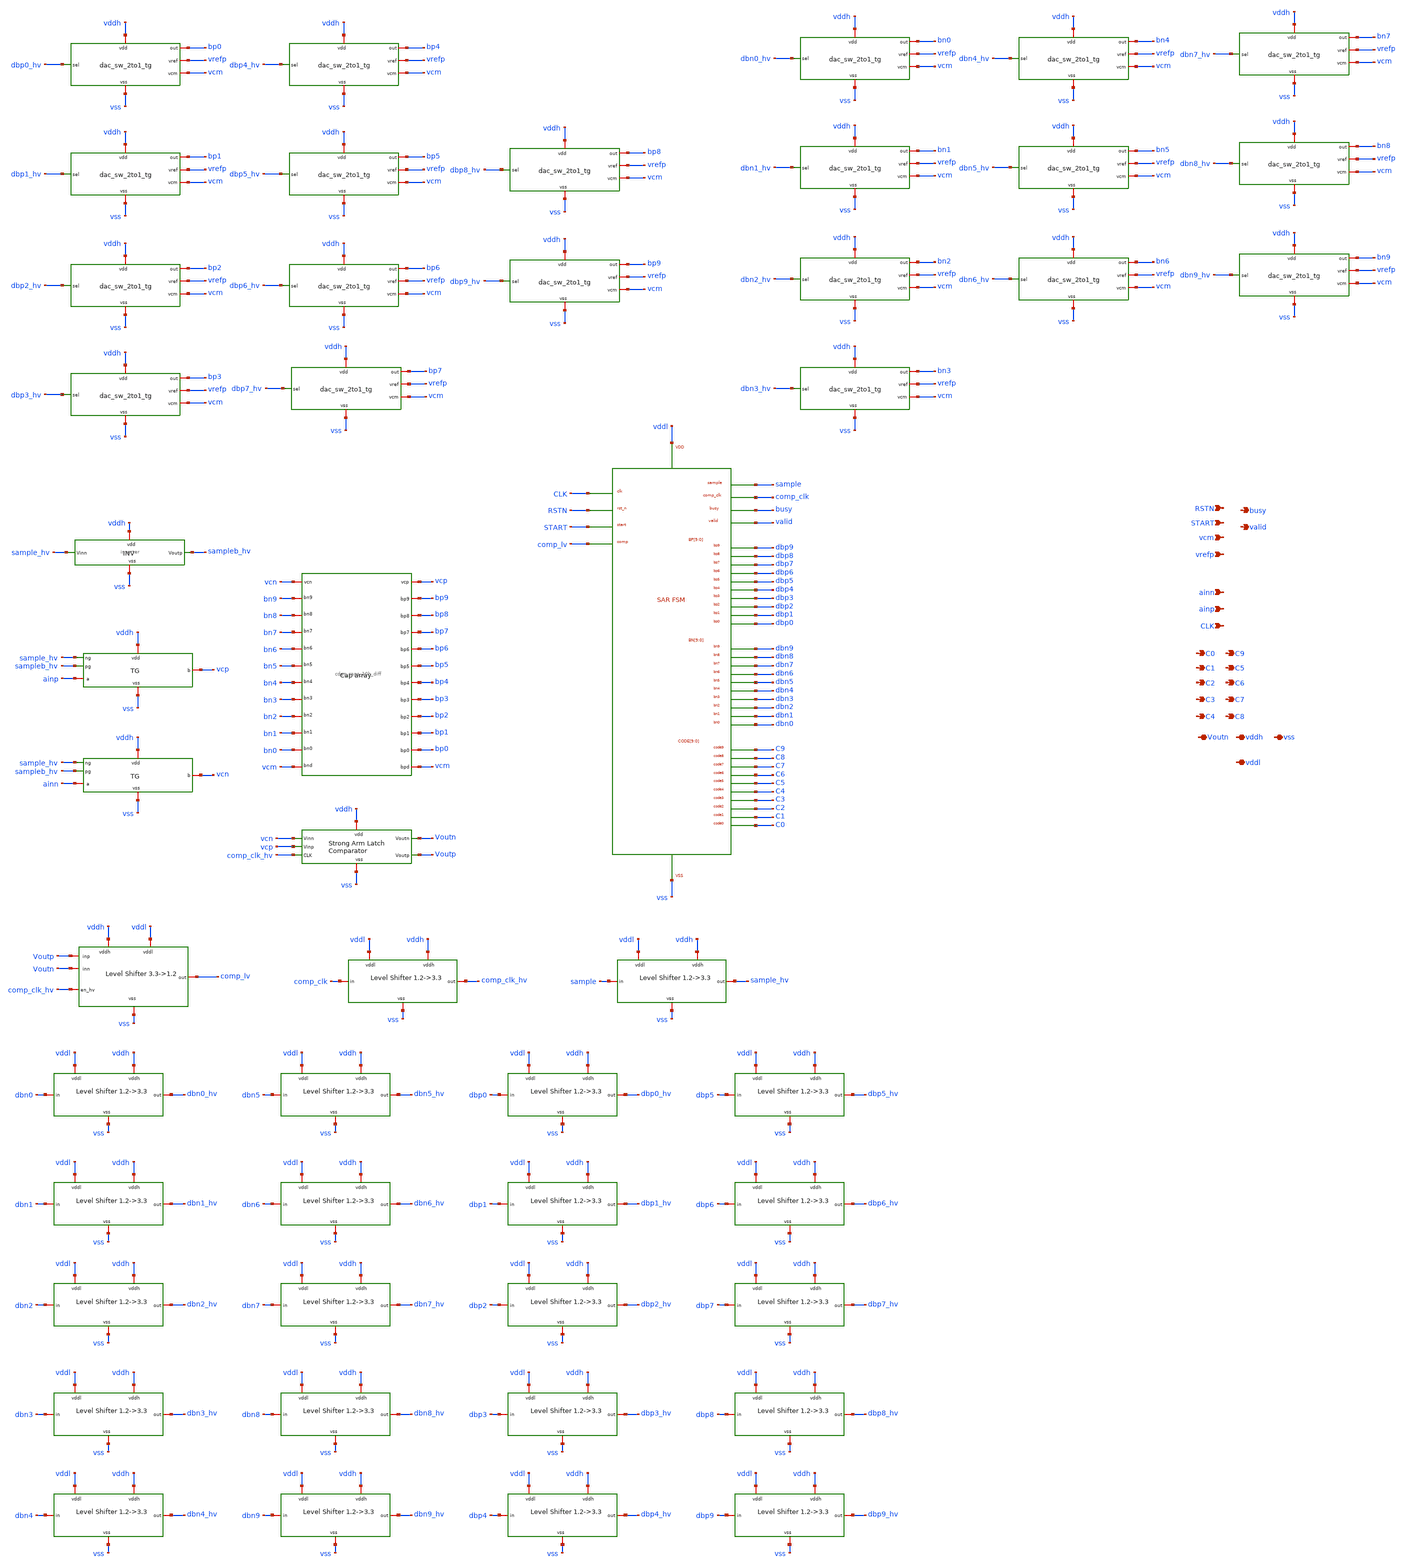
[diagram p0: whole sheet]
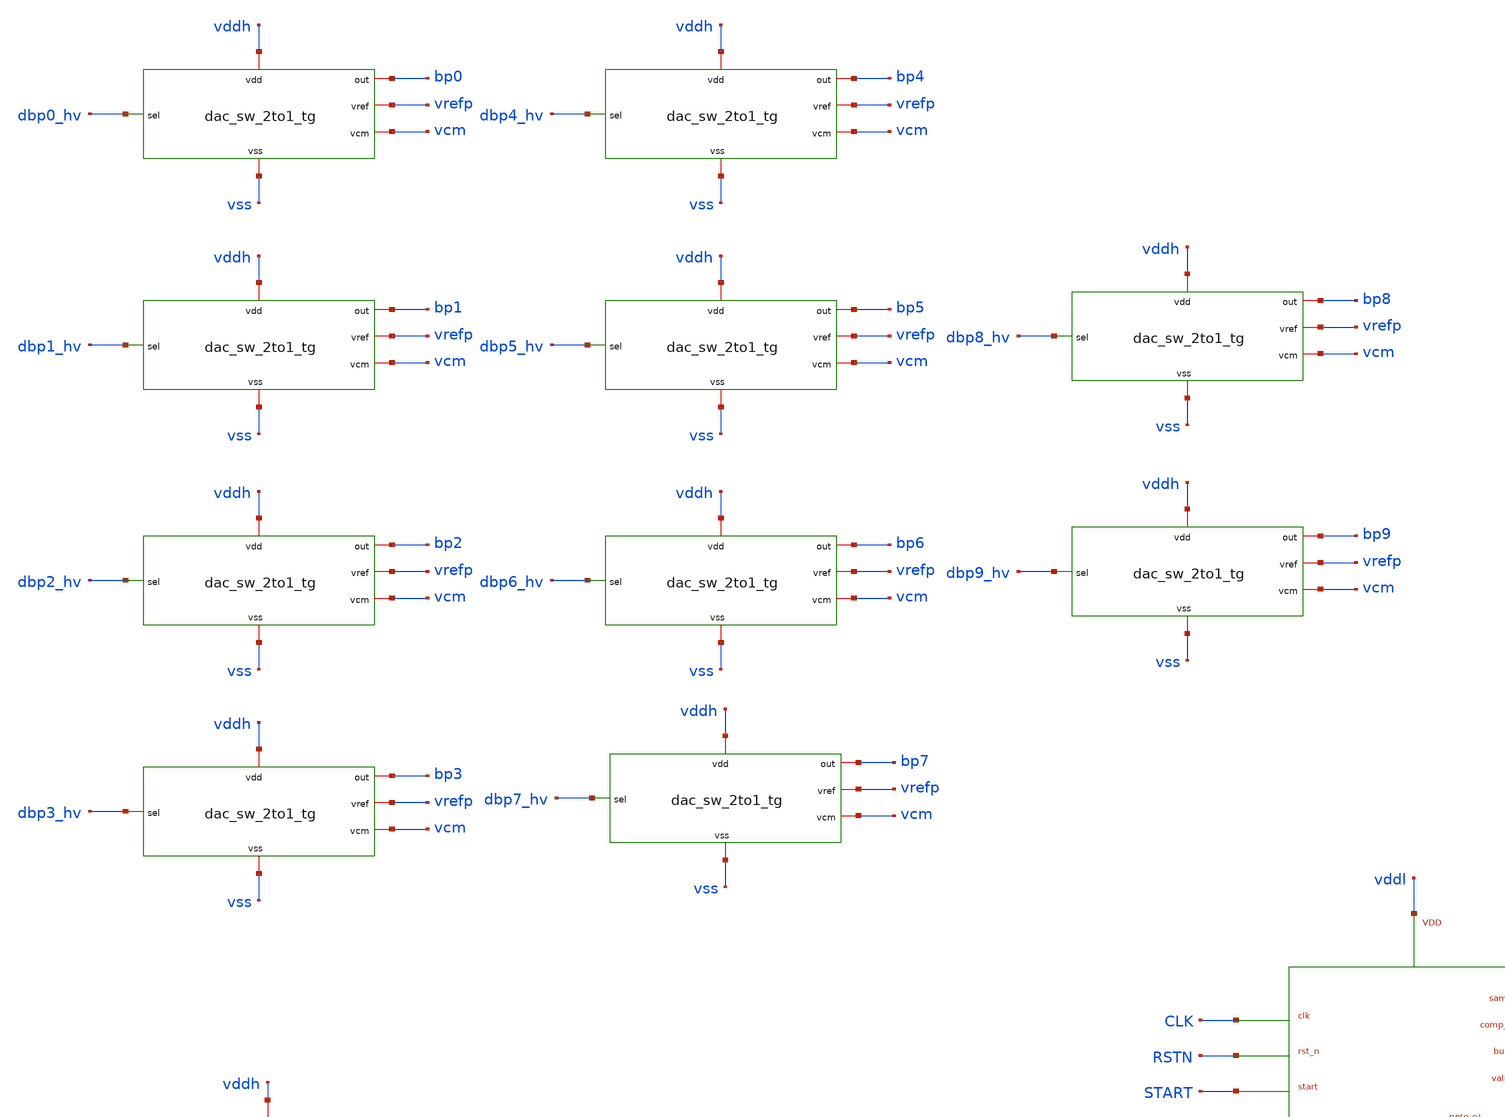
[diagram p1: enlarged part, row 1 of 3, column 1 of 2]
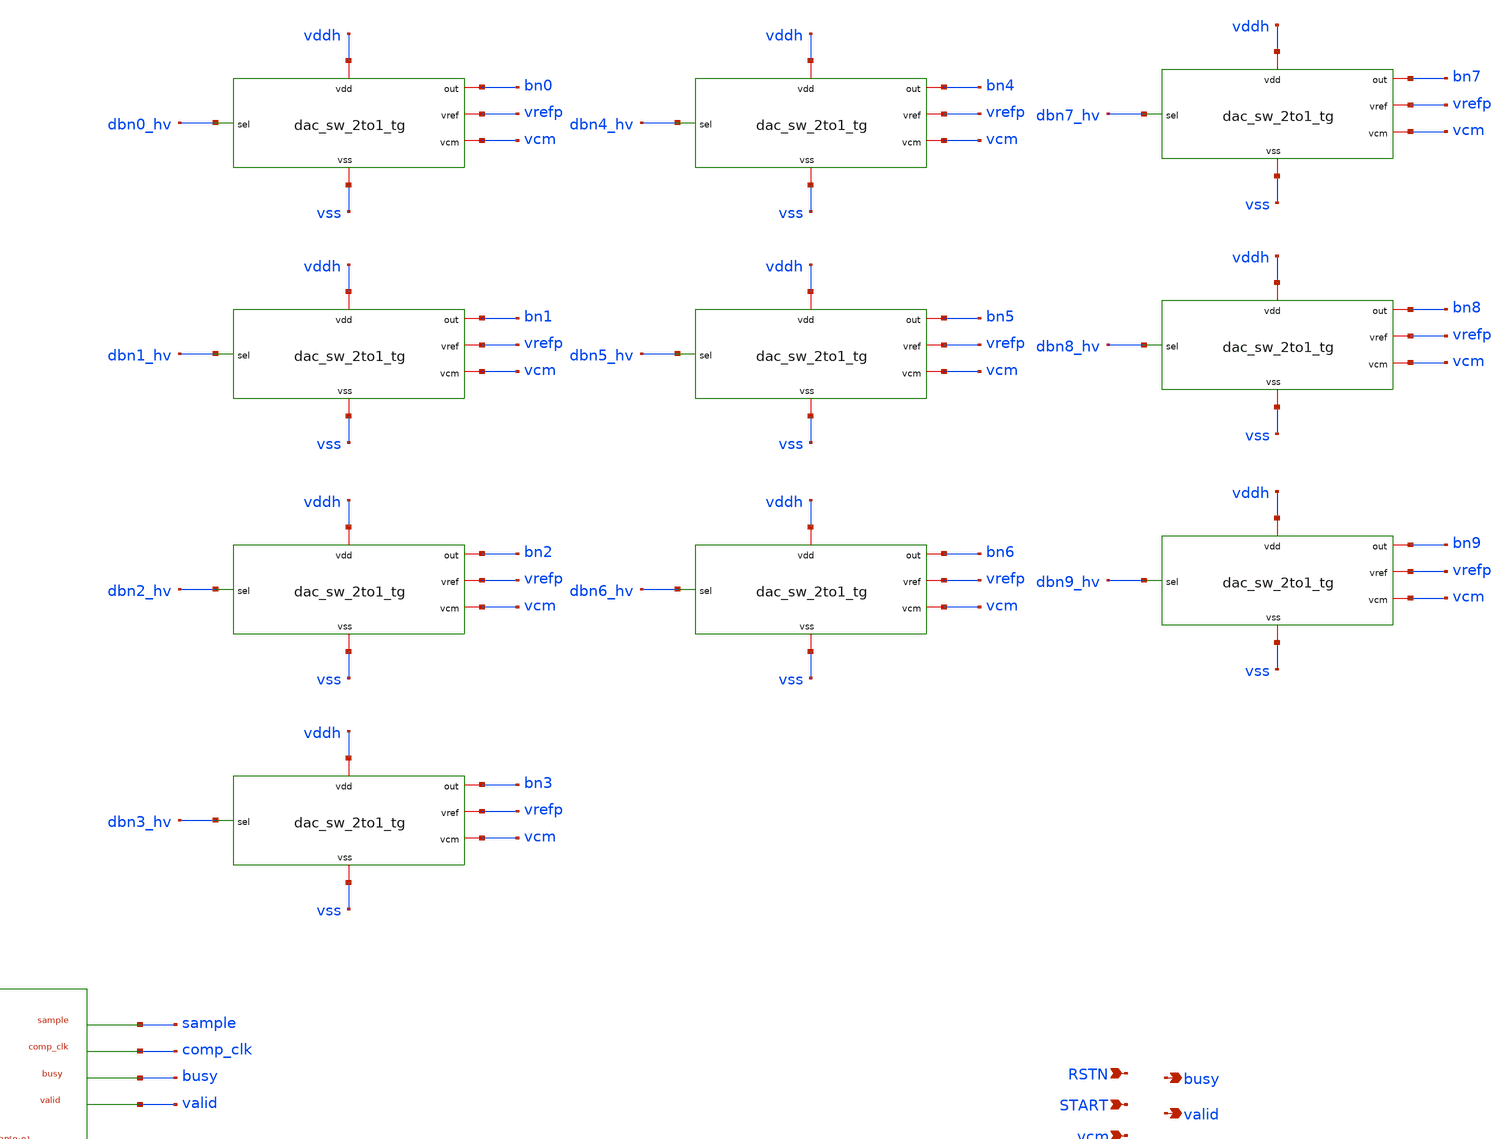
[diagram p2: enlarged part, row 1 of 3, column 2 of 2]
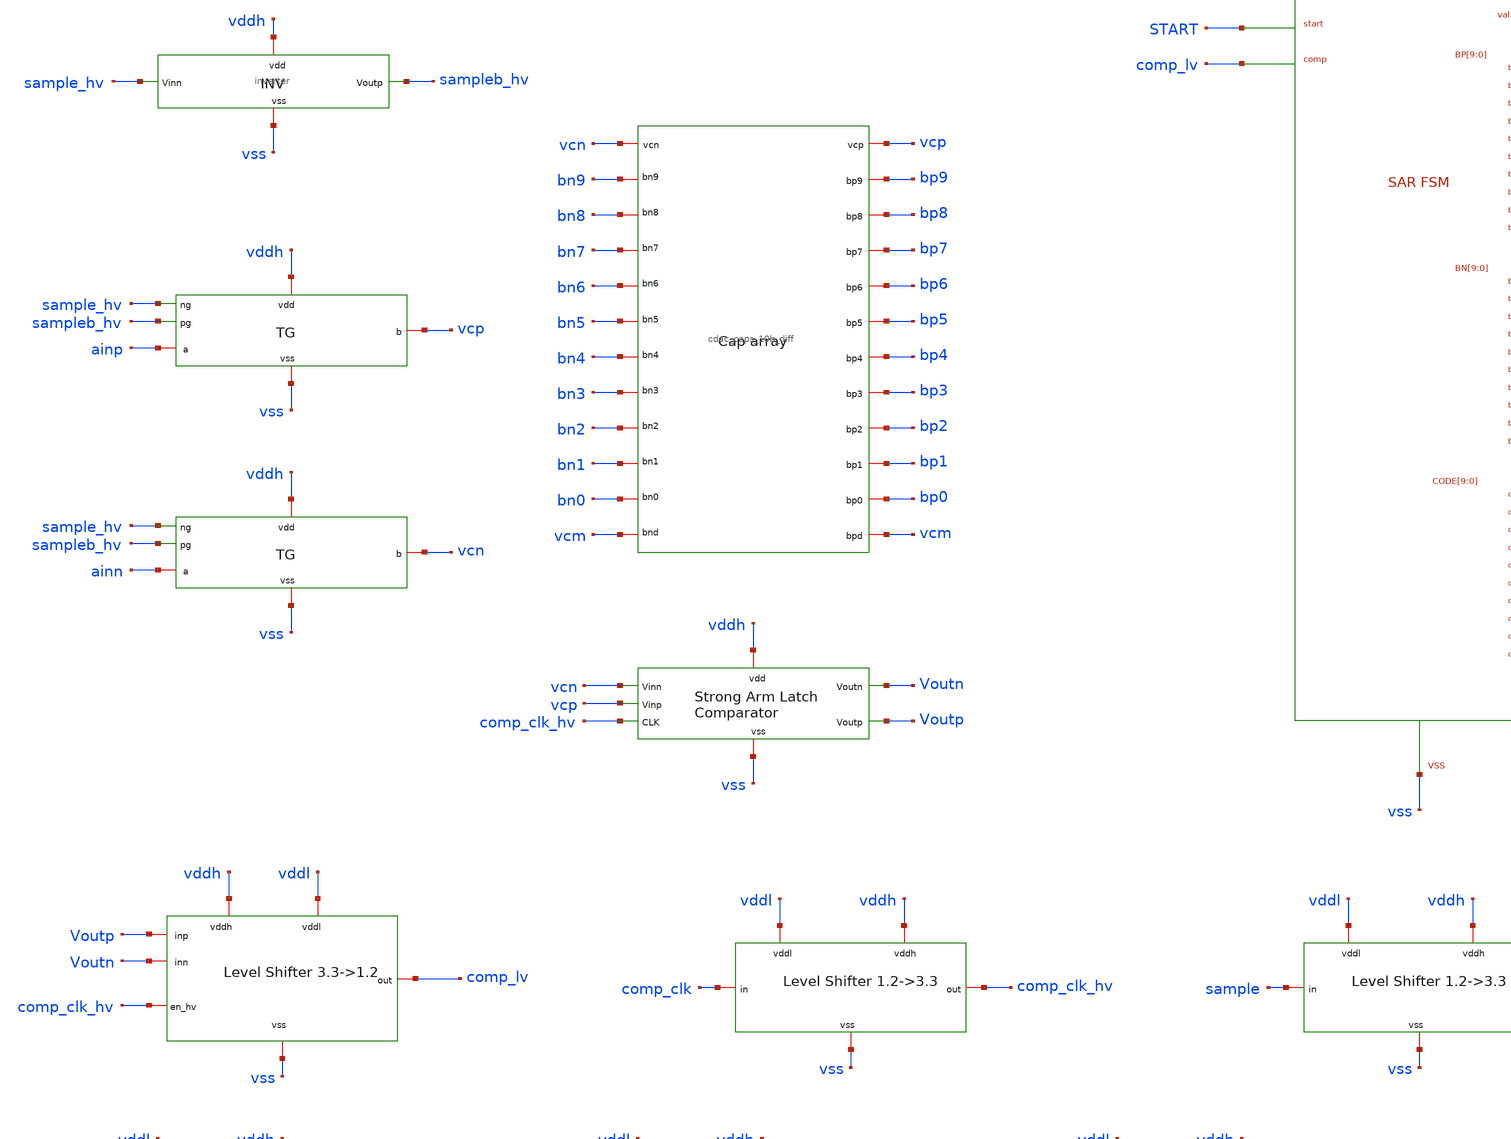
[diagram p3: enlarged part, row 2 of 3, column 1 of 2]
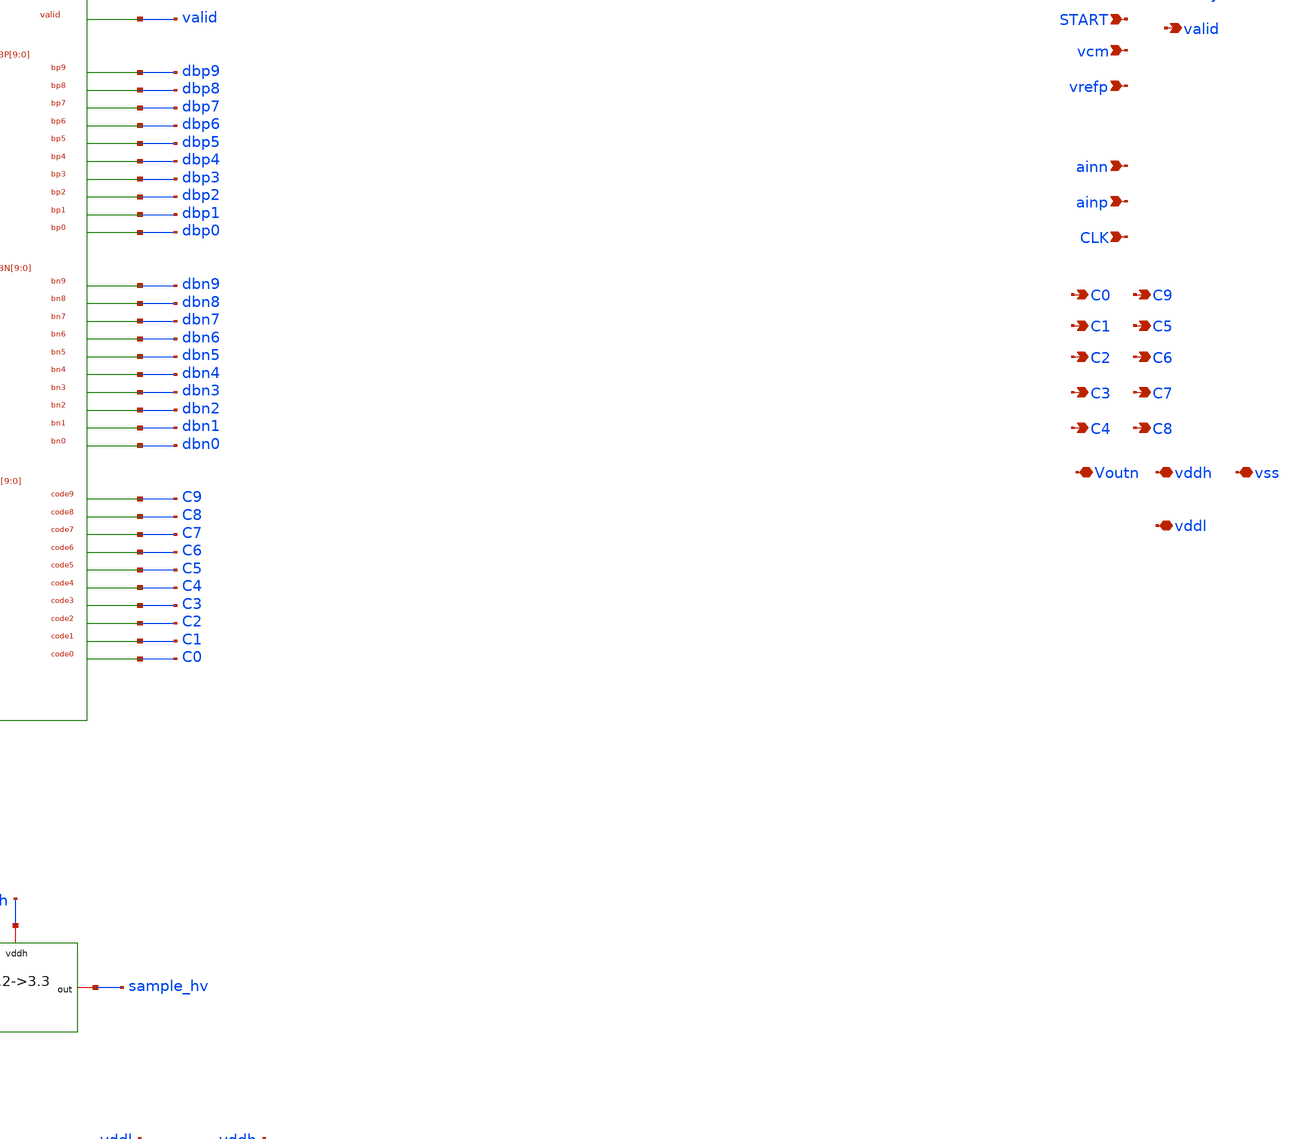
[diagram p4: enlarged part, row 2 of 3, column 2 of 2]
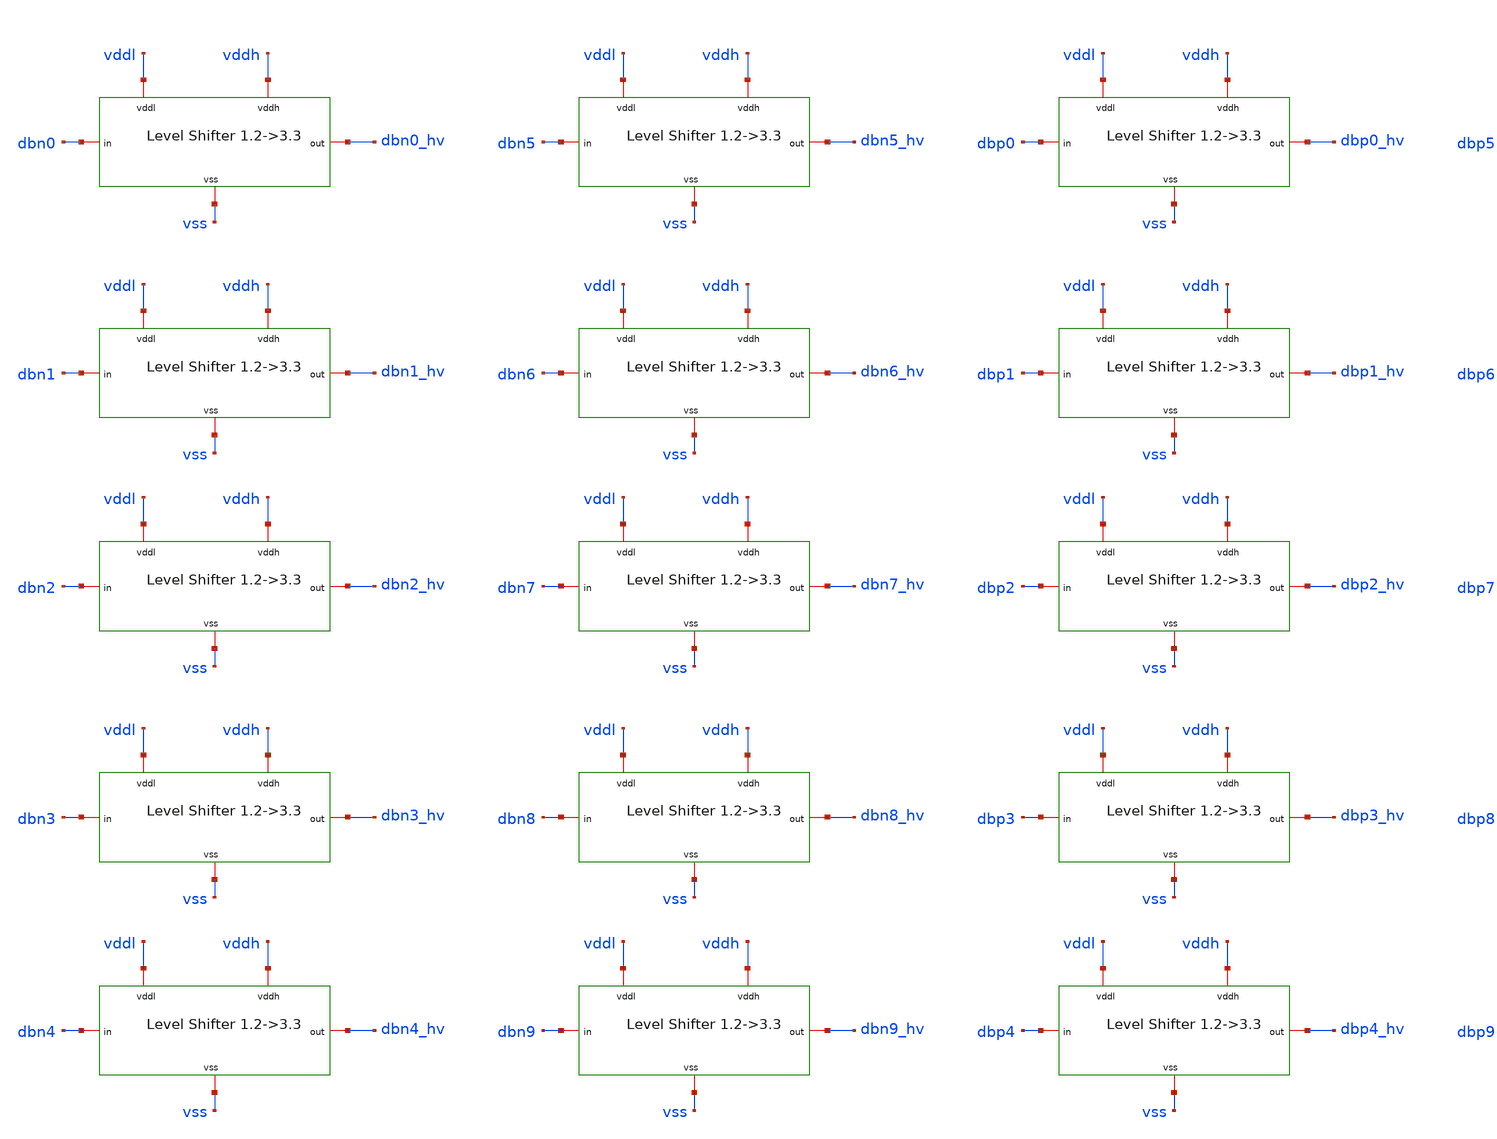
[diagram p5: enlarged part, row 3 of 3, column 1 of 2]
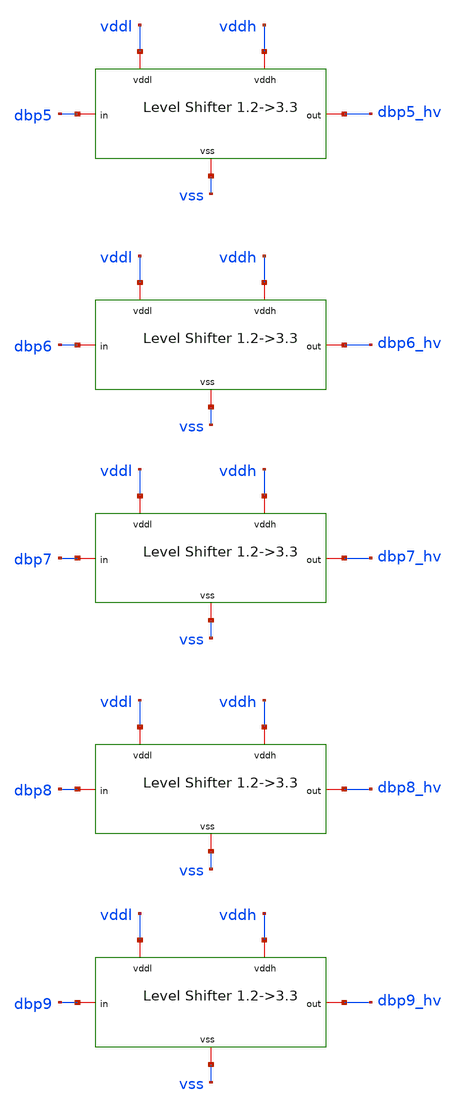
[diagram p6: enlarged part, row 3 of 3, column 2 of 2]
** sch_path: circuit_files/sar_adc_test/xschem/sar_10_bit.sch
**.subckt sar_10_bit ainn ainp CLK vrefp vcm C1 C2 C3 C4 C5 C6 C7 C8 C0 C9 busy valid START RSTN
*+ Voutn vddh vss vddl
*.ipin ainn
*.ipin ainp
*.ipin CLK
*.ipin vrefp
*.ipin vcm
*.opin C1
*.opin C2
*.opin C3
*.opin C4
*.opin C5
*.opin C6
*.opin C7
*.opin C8
*.opin C0
*.opin C9
*.opin busy
*.opin valid
*.ipin START
*.ipin RSTN
*.iopin Voutn
*.iopin vddh
*.iopin vss
*.iopin vddl
x1 Voutn vcn Voutp vcp vddh vss comp_clk_hv strong_arm_comp
x3 vss sample_hv sampleb_hv vddh ainp vcp tg
x4 vss sample_hv sampleb_hv vddh ainn vcn tg
x2 vcp bp3 bp0 bp5 bp2 vcm bp1 bp7 bp6 bp8 bp4 bp9 vcn bn0 bn1 bn8 bn7 bn6 bn5 bn4 bn3 bn9 bn2 vcm
+ cdac_caps_10b_diff
x15 vddh sample_hv sampleb_hv vss inverter
x6 dbp0_hv bp0 vss vddh vrefp vcm dac_sw_2to1_tg
x7 dbp1_hv bp1 vss vddh vrefp vcm dac_sw_2to1_tg
x8 dbp4_hv bp4 vss vddh vrefp vcm dac_sw_2to1_tg
x9 dbp5_hv bp5 vss vddh vrefp vcm dac_sw_2to1_tg
x10 dbp7_hv bp7 vss vddh vrefp vcm dac_sw_2to1_tg
x11 dbp8_hv bp8 vss vddh vrefp vcm dac_sw_2to1_tg
x12 dbp2_hv bp2 vss vddh vrefp vcm dac_sw_2to1_tg
x13 dbp3_hv bp3 vss vddh vrefp vcm dac_sw_2to1_tg
x14 dbp6_hv bp6 vss vddh vrefp vcm dac_sw_2to1_tg
x16 dbp9_hv bp9 vss vddh vrefp vcm dac_sw_2to1_tg
x17 dbn0_hv bn0 vss vddh vrefp vcm dac_sw_2to1_tg
x18 dbn1_hv bn1 vss vddh vrefp vcm dac_sw_2to1_tg
x19 dbn4_hv bn4 vss vddh vrefp vcm dac_sw_2to1_tg
x20 dbn5_hv bn5 vss vddh vrefp vcm dac_sw_2to1_tg
x21 dbn7_hv bn7 vss vddh vrefp vcm dac_sw_2to1_tg
x22 dbn8_hv bn8 vss vddh vrefp vcm dac_sw_2to1_tg
x23 dbn2_hv bn2 vss vddh vrefp vcm dac_sw_2to1_tg
x24 dbn3_hv bn3 vss vddh vrefp vcm dac_sw_2to1_tg
x25 dbn6_hv bn6 vss vddh vrefp vcm dac_sw_2to1_tg
x27 dbn9_hv bn9 vss vddh vrefp vcm dac_sw_2to1_tg
x5 CLK RSTN START comp_lv sample comp_clk busy valid dbp9 dbp8 dbp7 dbp6 dbp5 dbp4 dbp3 dbp2 dbp1
+ dbp0 dbn9 dbn8 dbn7 dbn6 dbn5 dbn4 dbn3 dbn2 dbn1 dbn0 C9 C8 C7 C6 C5 C4 C3 C2 C1 C0 vddl vss
+ sar_fsm_wrapper
x26 vss vddl vddh comp_lv Voutp Voutn comp_clk_hv level_shifter_3v3_to_1v2
x28 vss vddl vddh comp_clk_hv comp_clk level_shifter_1v2_to_3v3
x29 vss vddl vddh sample_hv sample level_shifter_1v2_to_3v3
x30 vss vddl vddh dbp0_hv dbp0 level_shifter_1v2_to_3v3
x31 vss vddl vddh dbp1_hv dbp1 level_shifter_1v2_to_3v3
x32 vss vddl vddh dbp5_hv dbp5 level_shifter_1v2_to_3v3
x33 vss vddl vddh dbp6_hv dbp6 level_shifter_1v2_to_3v3
x34 vss vddl vddh dbp2_hv dbp2 level_shifter_1v2_to_3v3
x35 vss vddl vddh dbp3_hv dbp3 level_shifter_1v2_to_3v3
x36 vss vddl vddh dbp7_hv dbp7 level_shifter_1v2_to_3v3
x37 vss vddl vddh dbp8_hv dbp8 level_shifter_1v2_to_3v3
x38 vss vddl vddh dbp4_hv dbp4 level_shifter_1v2_to_3v3
x39 vss vddl vddh dbp9_hv dbp9 level_shifter_1v2_to_3v3
x40 vss vddl vddh dbn0_hv dbn0 level_shifter_1v2_to_3v3
x41 vss vddl vddh dbn1_hv dbn1 level_shifter_1v2_to_3v3
x42 vss vddl vddh dbn5_hv dbn5 level_shifter_1v2_to_3v3
x43 vss vddl vddh dbn6_hv dbn6 level_shifter_1v2_to_3v3
x44 vss vddl vddh dbn2_hv dbn2 level_shifter_1v2_to_3v3
x45 vss vddl vddh dbn3_hv dbn3 level_shifter_1v2_to_3v3
x46 vss vddl vddh dbn7_hv dbn7 level_shifter_1v2_to_3v3
x47 vss vddl vddh dbn8_hv dbn8 level_shifter_1v2_to_3v3
x48 vss vddl vddh dbn4_hv dbn4 level_shifter_1v2_to_3v3
x49 vss vddl vddh dbn9_hv dbn9 level_shifter_1v2_to_3v3
**.ends
.end
